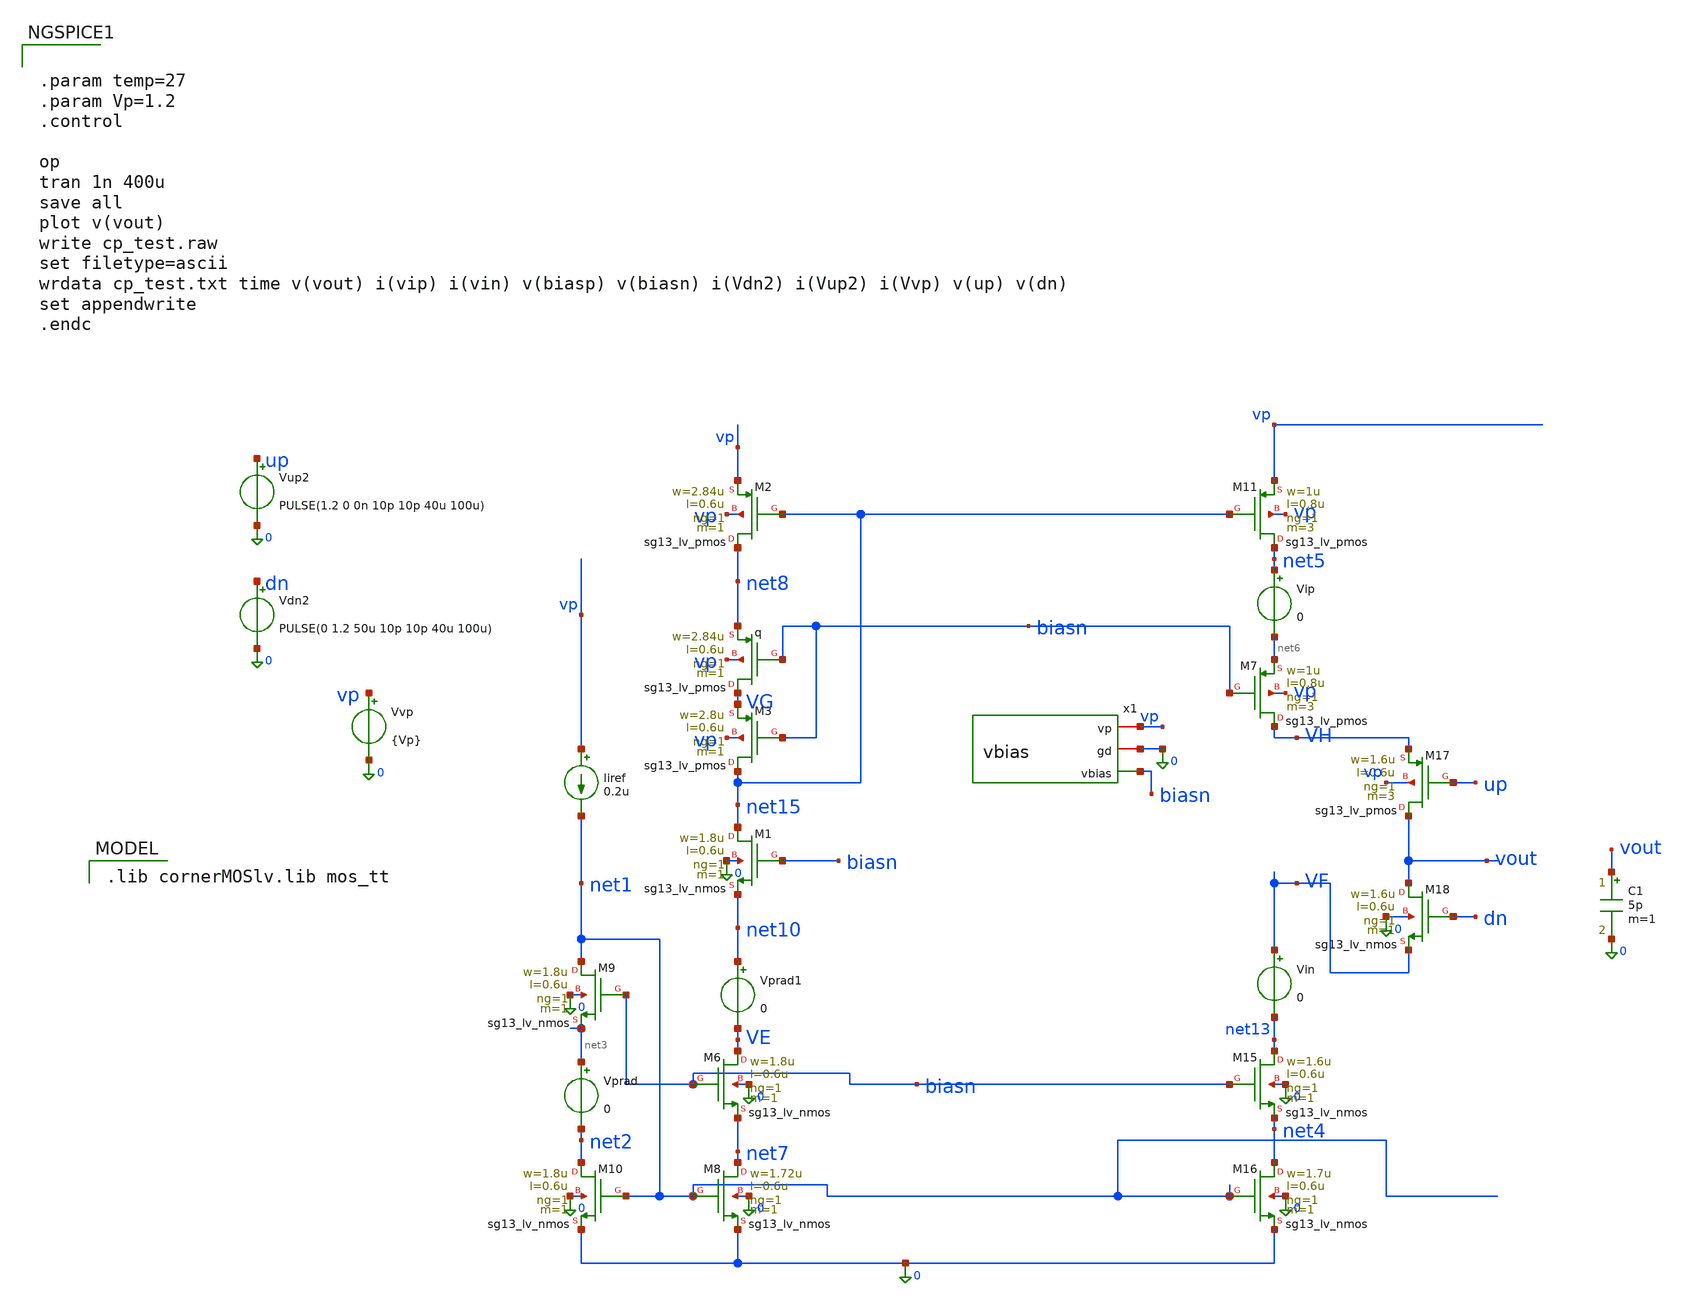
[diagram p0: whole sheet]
** sch_path: charge_pump/NEW_500n_tran_tb.sch
**.subckt NEW_500n_tran_tb
XM15 net13 biasn net4 0 sg13_lv_nmos w=1.6u l=0.6u ng=1 m=1 mm_ok=1
XM16 net4 net1 0 0 sg13_lv_nmos w=1.7u l=0.6u ng=1 m=1 mm_ok=1
XM1 net15 biasn net10 0 sg13_lv_nmos w=1.8u l=0.6u ng=1 m=1 mm_ok=1
XM6 VE biasn net7 0 sg13_lv_nmos w=1.8u l=0.6u ng=1 m=1 mm_ok=1
XM8 net7 net1 0 0 sg13_lv_nmos w=1.72u l=0.6u ng=1 m=1 mm_ok=1
XM9 net1 biasn net3 0 sg13_lv_nmos w=1.8u l=0.6u ng=1 m=1 mm_ok=1
XM10 net2 net1 0 0 sg13_lv_nmos w=1.8u l=0.6u ng=1 m=1 mm_ok=1
Vvp vp 0 {Vp}
Iiref vp net1 0.2u
Vprad net3 net2 0
Vprad1 net10 VE 0
Vin VF net13 0
Xq VG biasn net8 vp sg13_lv_pmos w=2.84u l=0.6u ng=1 m=1 mm_ok=1
XM3 net15 biasn VG vp sg13_lv_pmos w=2.8u l=0.6u ng=1 m=1 mm_ok=1
XM7 VH biasn net6 vp sg13_lv_pmos w=1u l=0.8u ng=1 m=3 mm_ok=1
XM11 net5 net15 vp vp sg13_lv_pmos w=1u l=0.8u ng=1 m=3 mm_ok=1
Vip net5 net6 0
XM2 net8 net15 vp vp sg13_lv_pmos w=2.84u l=0.6u ng=1 m=1 mm_ok=1
XM17 vout up VH vp sg13_lv_pmos w=1.6u l=0.6u ng=1 m=3 mm_ok=1
XM18 vout dn VF 0 sg13_lv_nmos w=1.6u l=0.6u ng=1 m=1 mm_ok=1
C1 vout 0 5p m=1
x1 vp 0 biasn vbias
Vup2 up 0 PULSE(1.2 0 0n 10p 10p 40u 100u)
Vdn2 dn 0 PULSE(0 1.2 50u 10p 10p 40u 100u)
**** begin user architecture code
 .lib cornerMOSlv.lib mos_tt



.param temp=27
.param Vp=1.2
.control

op
tran 1n 400u
save all
plot v(vout)
write cp_test.raw
set filetype=ascii
wrdata cp_test.txt time v(vout) i(vip) i(vin) v(biasp) v(biasn) i(Vdn2) i(Vup2) i(Vvp) v(up) v(dn)
set appendwrite
.endc


**** end user architecture code
**.ends

* expanding   symbol:  /foss/designs/CHIP-PLL/charge_pump/vbias.sym # of pins=3
** sym_path: schematics/charge_pump/vbias.sym
** sch_path: schematics/charge_pump/vbias.sch
.subckt vbias vp gd vbias
*.opin vbias
*.iopin gd
*.iopin vp
XM5 net1 iref vp vp sg13_lv_pmos w=1.2u l=0.6u ng=1 m=1 mm_ok=1
XM6 vbias net1 net2 gd sg13_lv_nmos w=3.6u l=0.6u ng=1 m=1 mm_ok=1
XM2 net2 net2 gd gd sg13_lv_nmos w=1.2u l=0.6u ng=1 m=1 mm_ok=1
XM3 gd gd gd gd sg13_lv_nmos w=1.86u l=0.6u ng=1 m=1 mm_ok=1
XM7 vp vp vp vp sg13_lv_pmos w=1.375u l=0.6u ng=1 m=1 mm_ok=1
XR1 net1 vbias gd rppd w=1e-6 l=1.7e-6 m=1 b=0 mm_ok=1
x1 vp iref gd curr_source
.ends


* expanding   symbol:  /foss/designs/CHIP-PLL/schematics/charge_pump/curr_source.sym # of pins=3
** sym_path: charge_pump/curr_source.sym
** sch_path: charge_pump/curr_source.sch
.subckt curr_source vp iref gd
*.iopin vp
*.iopin gd
*.opin iref
XM4 iref iref vp vp sg13_lv_pmos w=1.4u l=0.6u ng=1 m=1 mm_ok=1
XM5 net2 iref vp vp sg13_lv_pmos w=1.2u l=0.6u ng=1 m=1 mm_ok=1
XM6 net3 net3 gd gd sg13_lv_nmos w=1u l=0.6u ng=1 m=1 mm_ok=1
XM3 net2 net2 gd gd sg13_lv_nmos w=1.4u l=0.6u ng=1 m=1 mm_ok=1
XR2 net1 gd gd rppd w=1e-6 l=1.70e-6 m=1 b=0 mm_ok=1
XM1 iref net2 net1 gd sg13_lv_nmos w=1.2u l=0.6u ng=1 m=1 mm_ok=1
XM2 vp net3 iref gd sg13_lv_nmos w=1u l=0.6u ng=1 m=1 mm_ok=1
XM7 vp vp net3 gd sg13_lv_nmos w=1u l=0.6u ng=1 m=1 mm_ok=1
XM8 gd gd gd gd sg13_lv_nmos w=0.4u l=0.6u ng=1 m=1 mm_ok=1
.ends

.end
